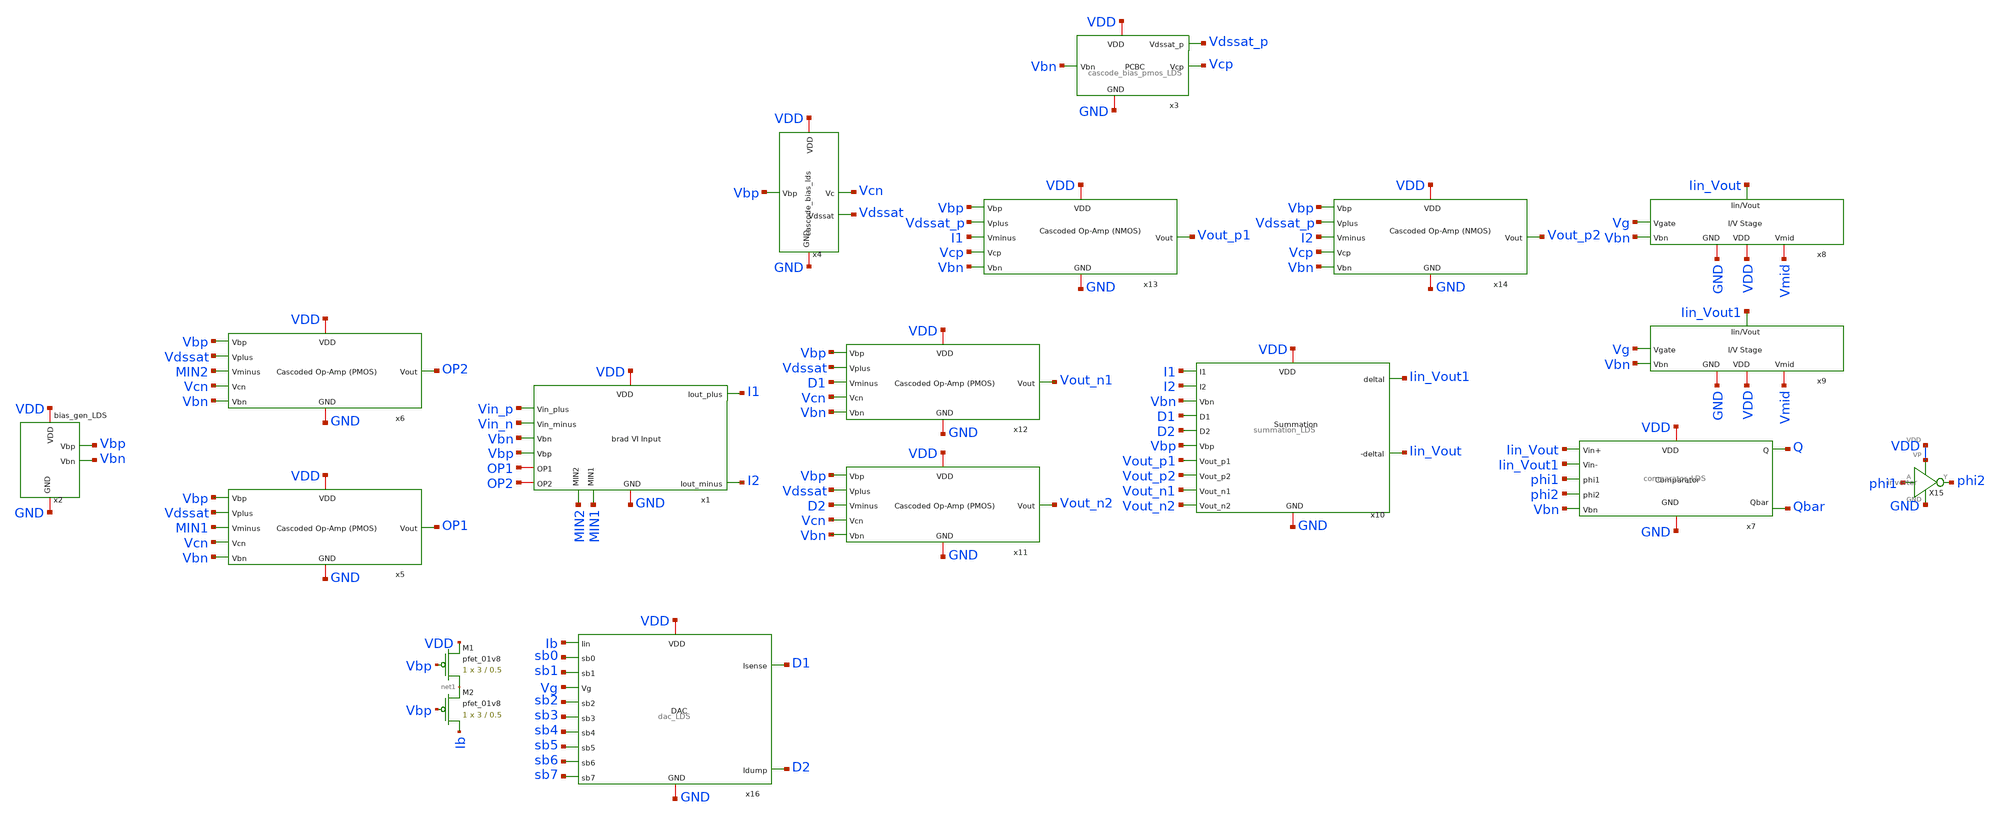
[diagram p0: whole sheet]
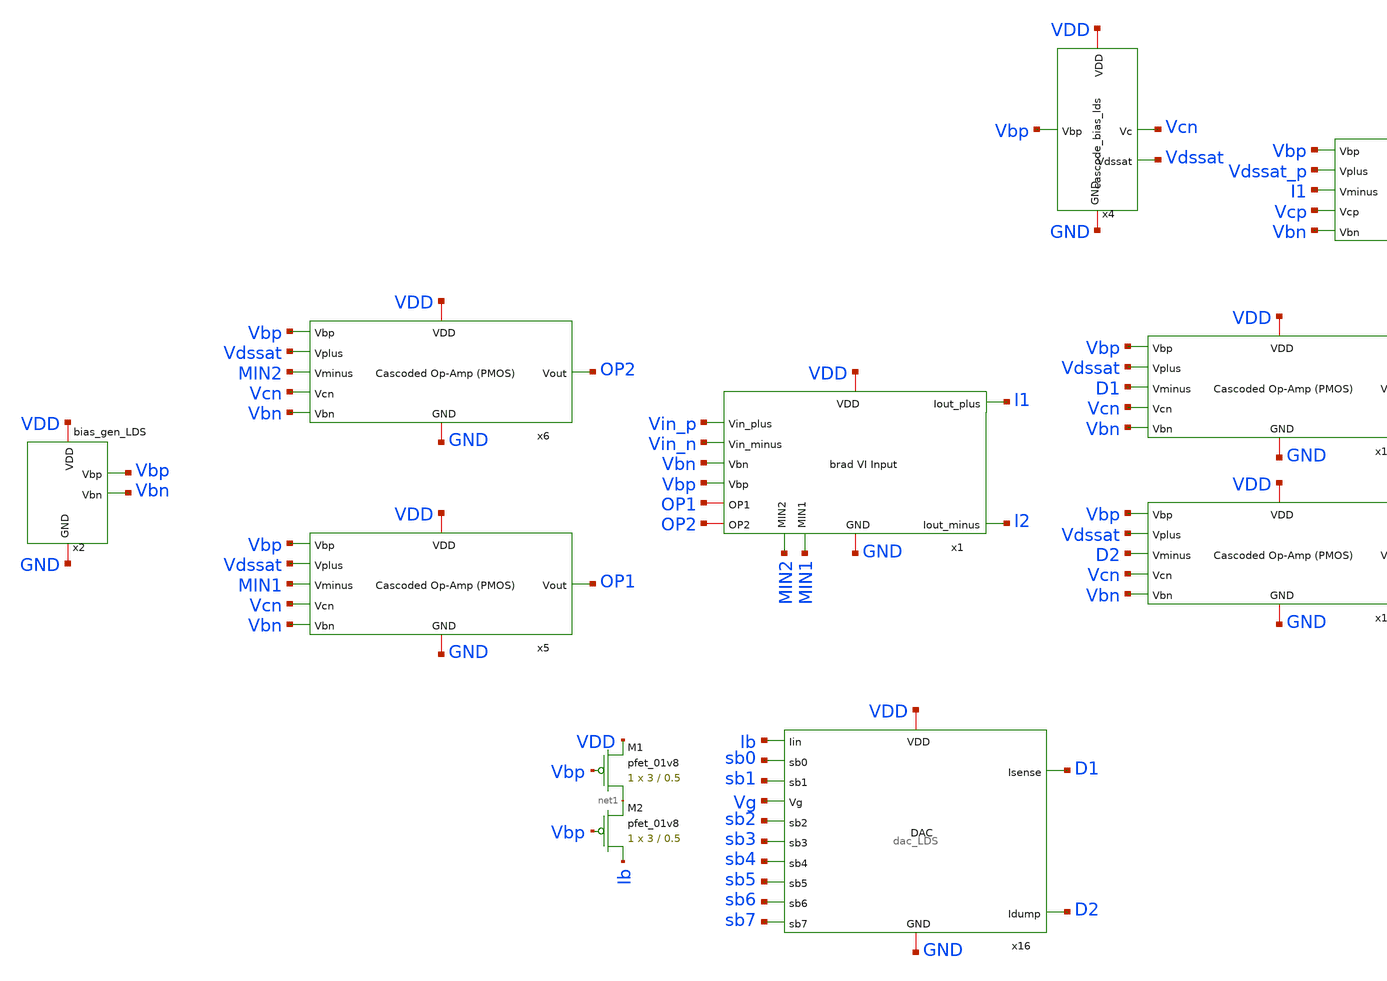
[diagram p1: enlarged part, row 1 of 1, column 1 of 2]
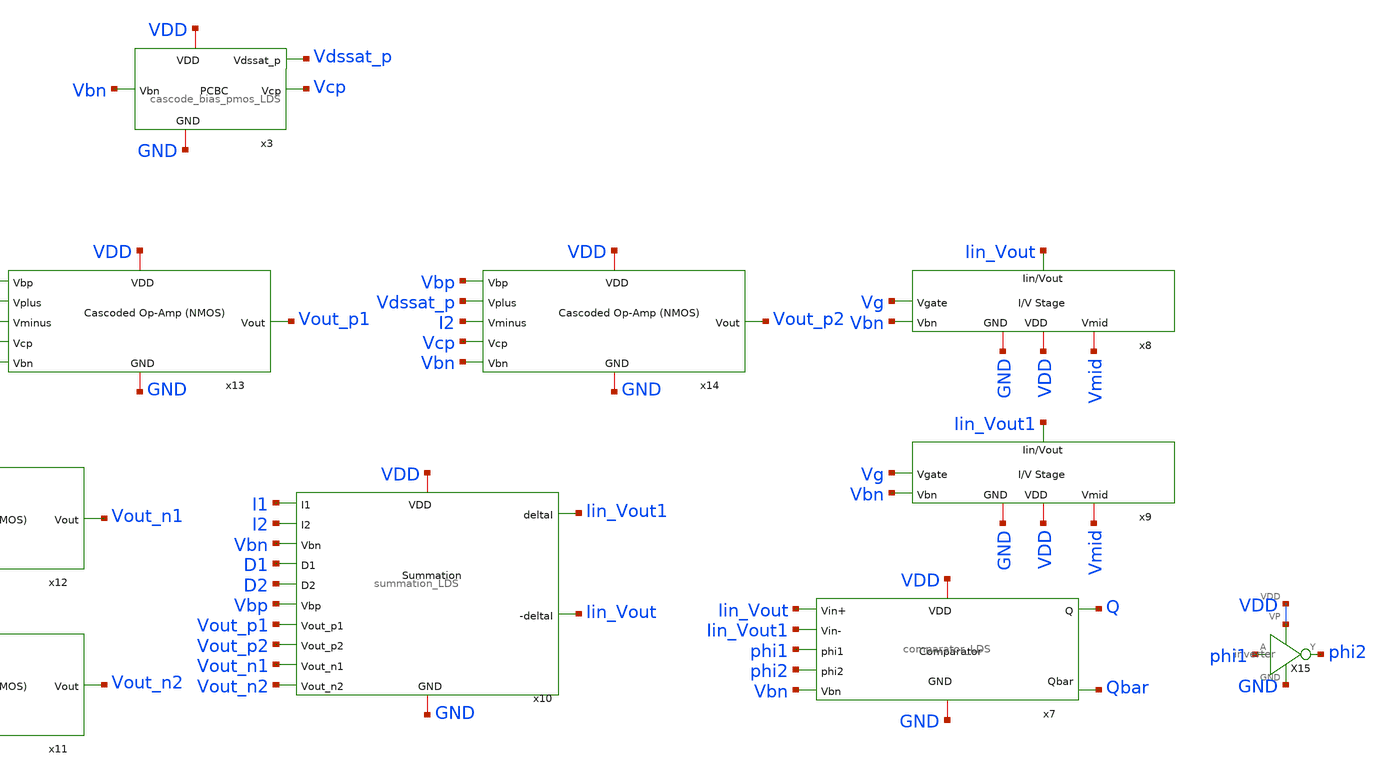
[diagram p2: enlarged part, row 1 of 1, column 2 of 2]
** sch_path: final/LDS/ADC_LDS.sch
**.subckt ADC_LDS
x1 VDD I1 I2 Vin_p Vin_n Vbn Vbp GND OP1 OP2 MIN1 MIN2 brad_VI_input_LDS
x2 VDD Vbp GND Vbn bias_gen_LDS
x3 Vbn VDD GND Vcp Vdssat_p cascode_bias_pmos_LDS
x4 Vbp VDD Vcn GND Vdssat cascode_bias_lds
x5 Vbp Vdssat MIN1 Vcn Vbn VDD GND OP1 cascoded_opamp_pmos_LDS
x6 Vbp Vdssat MIN2 Vcn Vbn VDD GND OP2 cascoded_opamp_pmos_LDS
x7 VDD Vbn Iin_Vout Iin_Vout1 phi1 phi2 Q Qbar GND comparator_LDS
x8 Iin_Vout Vg Vmid Vbn GND VDD IV_converter_LDS
x9 Iin_Vout1 Vg Vmid Vbn GND VDD IV_converter_LDS
x10 VDD GND I1 I2 Vbn D1 D2 Iin_Vout1 Iin_Vout Vbp Vout_p1 Vout_p2 Vout_n1 Vout_n2 summation_LDS
x11 Vbp Vdssat D2 Vcn Vbn VDD GND Vout_n2 cascoded_opamp_pmos_LDS
x12 Vbp Vdssat D1 Vcn Vbn VDD GND Vout_n1 cascoded_opamp_pmos_LDS
x13 Vbp Vdssat_p I1 Vcp Vbn VDD GND Vout_p1 cascoded_opamp_LDS
x14 Vbp Vdssat_p I2 Vcp Vbn VDD GND Vout_p2 cascoded_opamp_LDS
X15 VDD phi1 phi2 GND VDD inverter
x16 sb0 VDD GND sb1 Vg sb2 sb3 D1 sb4 D2 sb5 sb6 sb7 Ib dac_LDS
XM1 net1 Vbp VDD VDD sky130_fd_pr__pfet_01v8 L=0.5 W=3 nf=1 ad='int((nf+1)/2) * W/nf * 0.29' as='int((nf+2)/2) * W/nf * 0.29'
+ pd='2*int((nf+1)/2) * (W/nf + 0.29)' ps='2*int((nf+2)/2) * (W/nf + 0.29)' nrd='0.29 / W' nrs='0.29 / W'
+ sa=0 sb=0 sd=0 mult=1 m=1
XM2 Ib Vbp net1 VDD sky130_fd_pr__pfet_01v8 L=0.5 W=3 nf=1 ad='int((nf+1)/2) * W/nf * 0.29' as='int((nf+2)/2) * W/nf * 0.29'
+ pd='2*int((nf+1)/2) * (W/nf + 0.29)' ps='2*int((nf+2)/2) * (W/nf + 0.29)' nrd='0.29 / W' nrs='0.29 / W'
+ sa=0 sb=0 sd=0 mult=1 m=1
**.ends
.end
